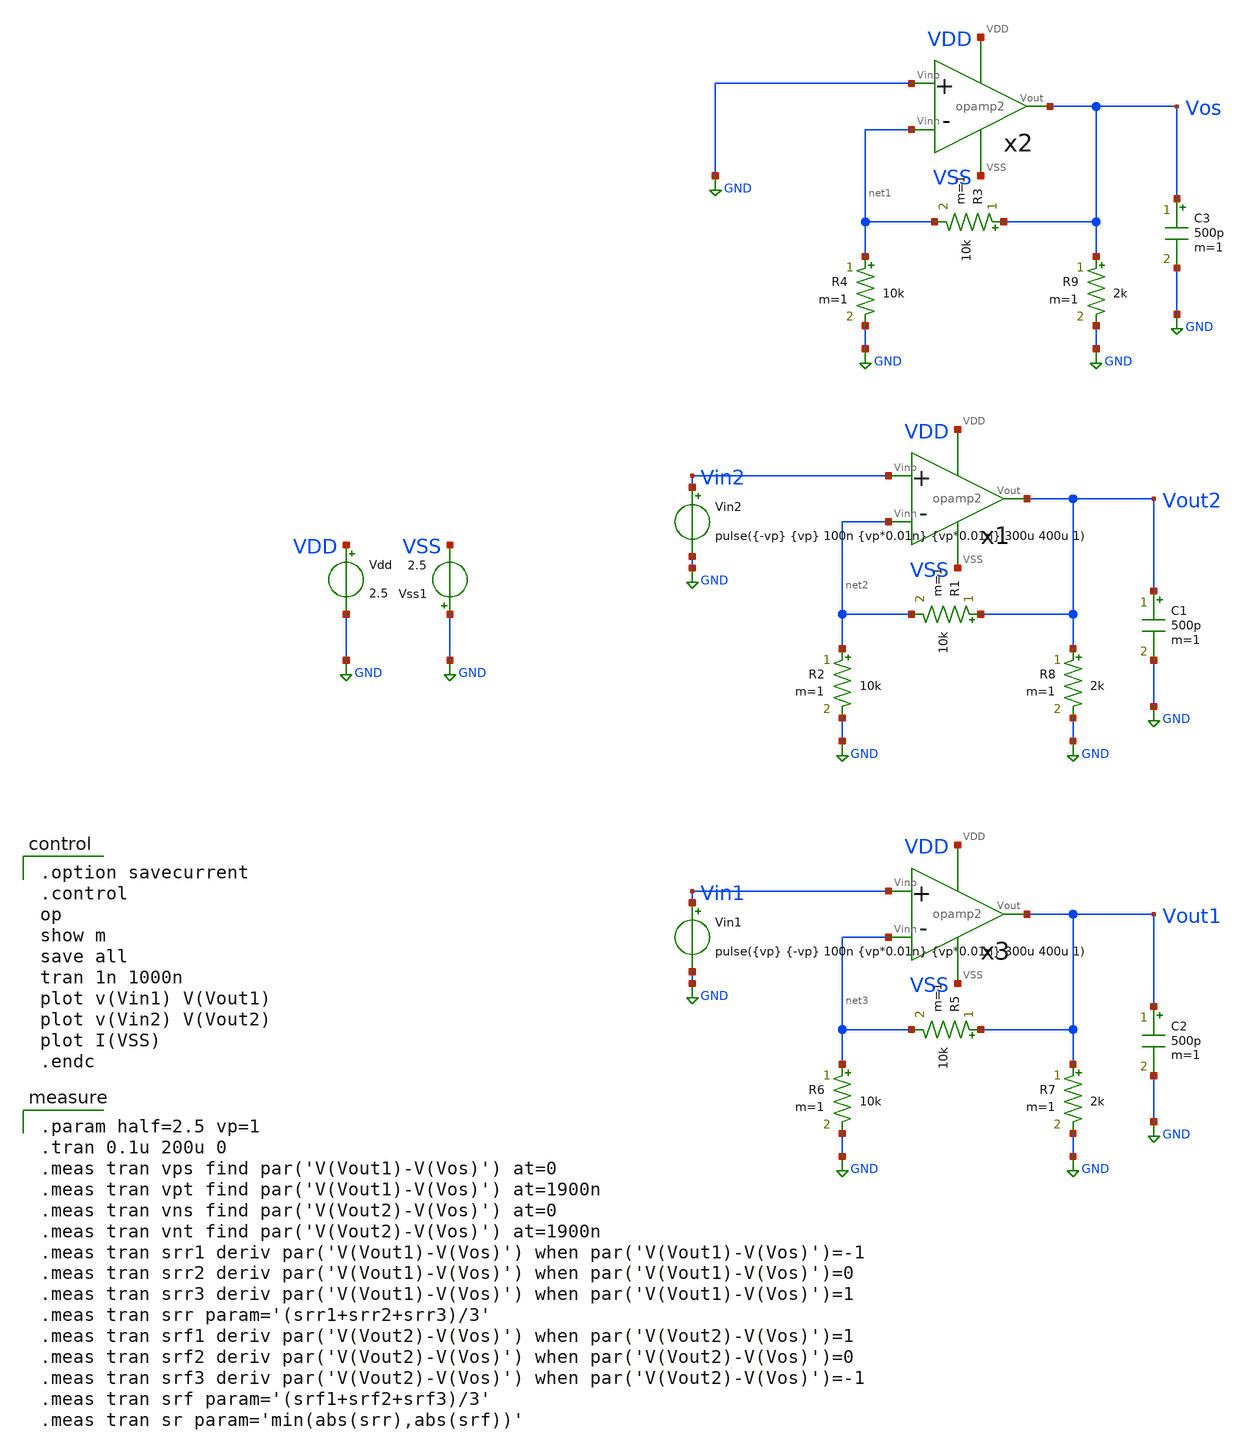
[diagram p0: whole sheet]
** sch_path: OPAF2026/opamp_sr.sch
**.subckt opamp_sr
Vdd VDD GND 2.5
Vss1 GND VSS 2.5
x2 GND net1 Vos VDD VSS opamp2
R3 Vos net1 10k m=1
R4 net1 GND 10k m=1
C3 Vos GND 500p m=1
x1 Vin2 net2 Vout2 VDD VSS opamp2
R1 Vout2 net2 10k m=1
R2 net2 GND 10k m=1
C1 Vout2 GND 500p m=1
Vin2 Vin2 GND pulse({-vp} {vp} 100n {vp*0.01n} {vp*0.01n} 300u 400u 1)
x3 Vin1 net3 Vout1 VDD VSS opamp2
R5 Vout1 net3 10k m=1
R6 net3 GND 10k m=1
C2 Vout1 GND 500p m=1
Vin1 Vin1 GND pulse({vp} {-vp} 100n {vp*0.01n} {vp*0.01n} 300u 400u 1)
R7 Vout1 GND 2k m=1
R8 Vout2 GND 2k m=1
R9 Vos GND 2k m=1
**** begin user architecture code

.option savecurrent
.control
op
show m
save all
tran 1n 1000n
plot v(Vin1) V(Vout1)
plot v(Vin2) V(Vout2)
plot I(VSS)
.endc


.param half=2.5 vp=1
.tran 0.1u 200u 0
.meas tran vps find par('V(Vout1)-V(Vos)') at=0
.meas tran vpt find par('V(Vout1)-V(Vos)') at=1900n
.meas tran vns find par('V(Vout2)-V(Vos)') at=0
.meas tran vnt find par('V(Vout2)-V(Vos)') at=1900n
.meas tran srr1 deriv par('V(Vout1)-V(Vos)') when par('V(Vout1)-V(Vos)')=-1
.meas tran srr2 deriv par('V(Vout1)-V(Vos)') when par('V(Vout1)-V(Vos)')=0
.meas tran srr3 deriv par('V(Vout1)-V(Vos)') when par('V(Vout1)-V(Vos)')=1
.meas tran srr param='(srr1+srr2+srr3)/3'
.meas tran srf1 deriv par('V(Vout2)-V(Vos)') when par('V(Vout2)-V(Vos)')=1
.meas tran srf2 deriv par('V(Vout2)-V(Vos)') when par('V(Vout2)-V(Vos)')=0
.meas tran srf3 deriv par('V(Vout2)-V(Vos)') when par('V(Vout2)-V(Vos)')=-1
.meas tran srf param='(srf1+srf2+srf3)/3'
.meas tran sr param='min(abs(srr),abs(srf))'

 .include $::LIB/ip62_models
**** end user architecture code
**.ends

* expanding   symbol:  /home/tsukiji_lab04/OPAF2026/opamp2.sym # of pins=5
** sym_path: OPAF2026/opamp2.sym
** sch_path: OPAF2026/opamp2.sch
.subckt opamp2 Vinp Vinn Vout VDD VSS
*.opin Vout
*.iopin VDD
*.iopin VSS
*.ipin Vinn
*.ipin Vinp
XXM1 net2 net1 VDD VDD PMOS w=50u l=1u nrd=0 nrs=0 m=1
XXM2 net1 net1 VDD VDD PMOS w=50u l=1u nrd=0 nrs=0 m=1
XXM3 net1 Vinn net3 VSS NMOS w=115u l=1u nrd=0 nrs=0 m=1
XXM4 net2 Vinp net3 VSS NMOS w=115u l=1u nrd=0 nrs=0 m=1
XXM5 Vout net2 VDD VDD PMOS w=1360u l=1u nrd=0 nrs=0 m=1
XXM6 net3 net4 VSS VSS NMOS w=175u l=1u nrd=0 nrs=0 m=1
XXM7 Vout net4 VSS VSS NMOS w=2440u l=1u nrd=0 nrs=0 m=1
XXM8 net4 net4 VSS VSS NMOS w=200u l=10u nrd=0 nrs=0 m=1
C1 net5 Vout 25p m=1
R1 VDD net4 58.70k m=1
R2 net2 net5 1k m=1
.ends

.GLOBAL GND
.end
